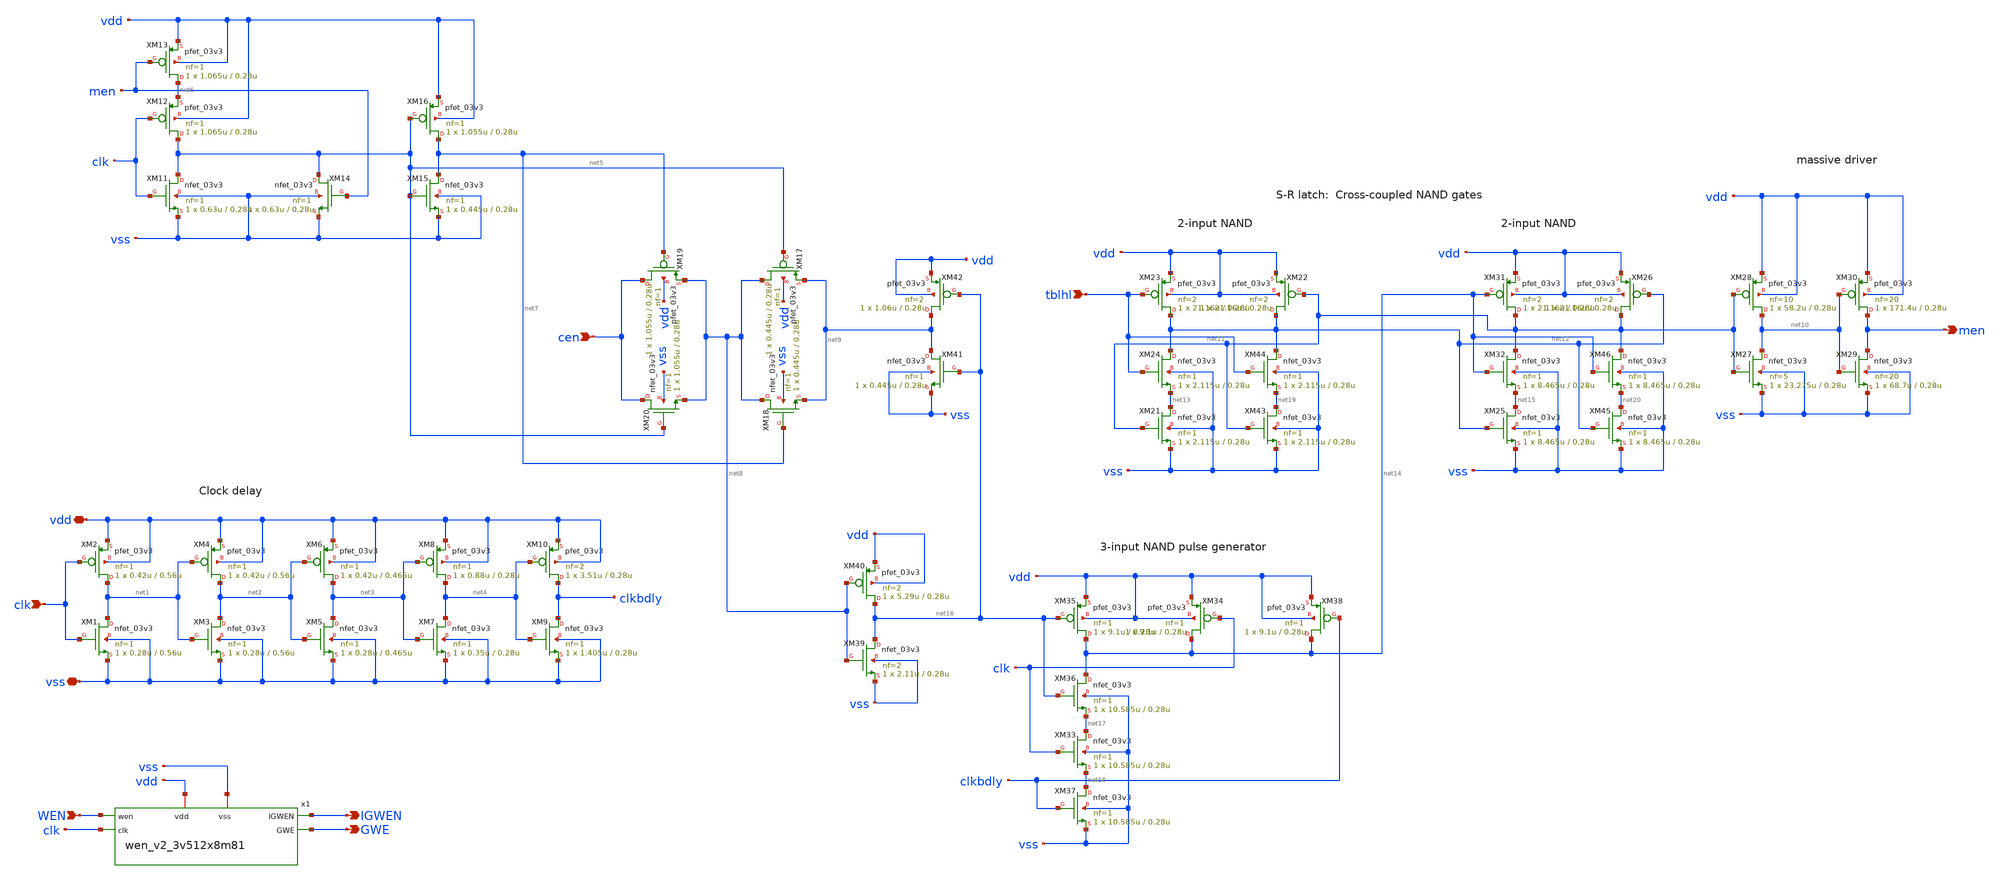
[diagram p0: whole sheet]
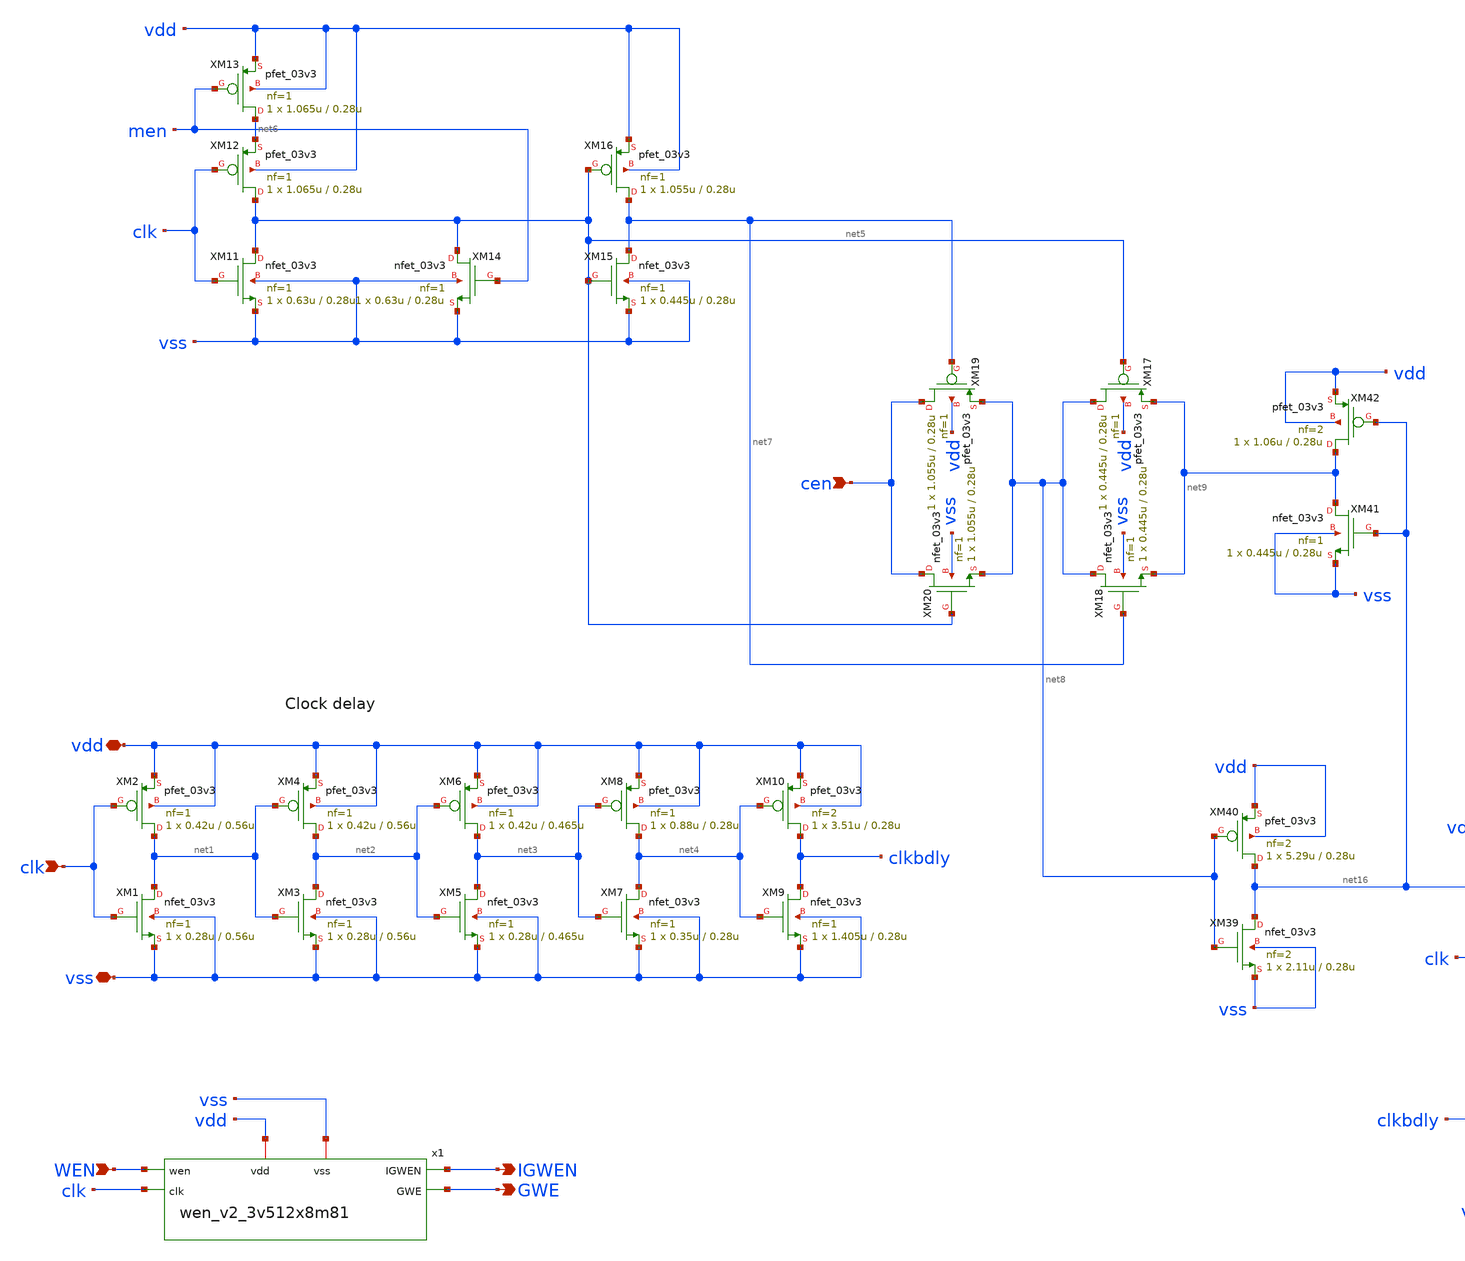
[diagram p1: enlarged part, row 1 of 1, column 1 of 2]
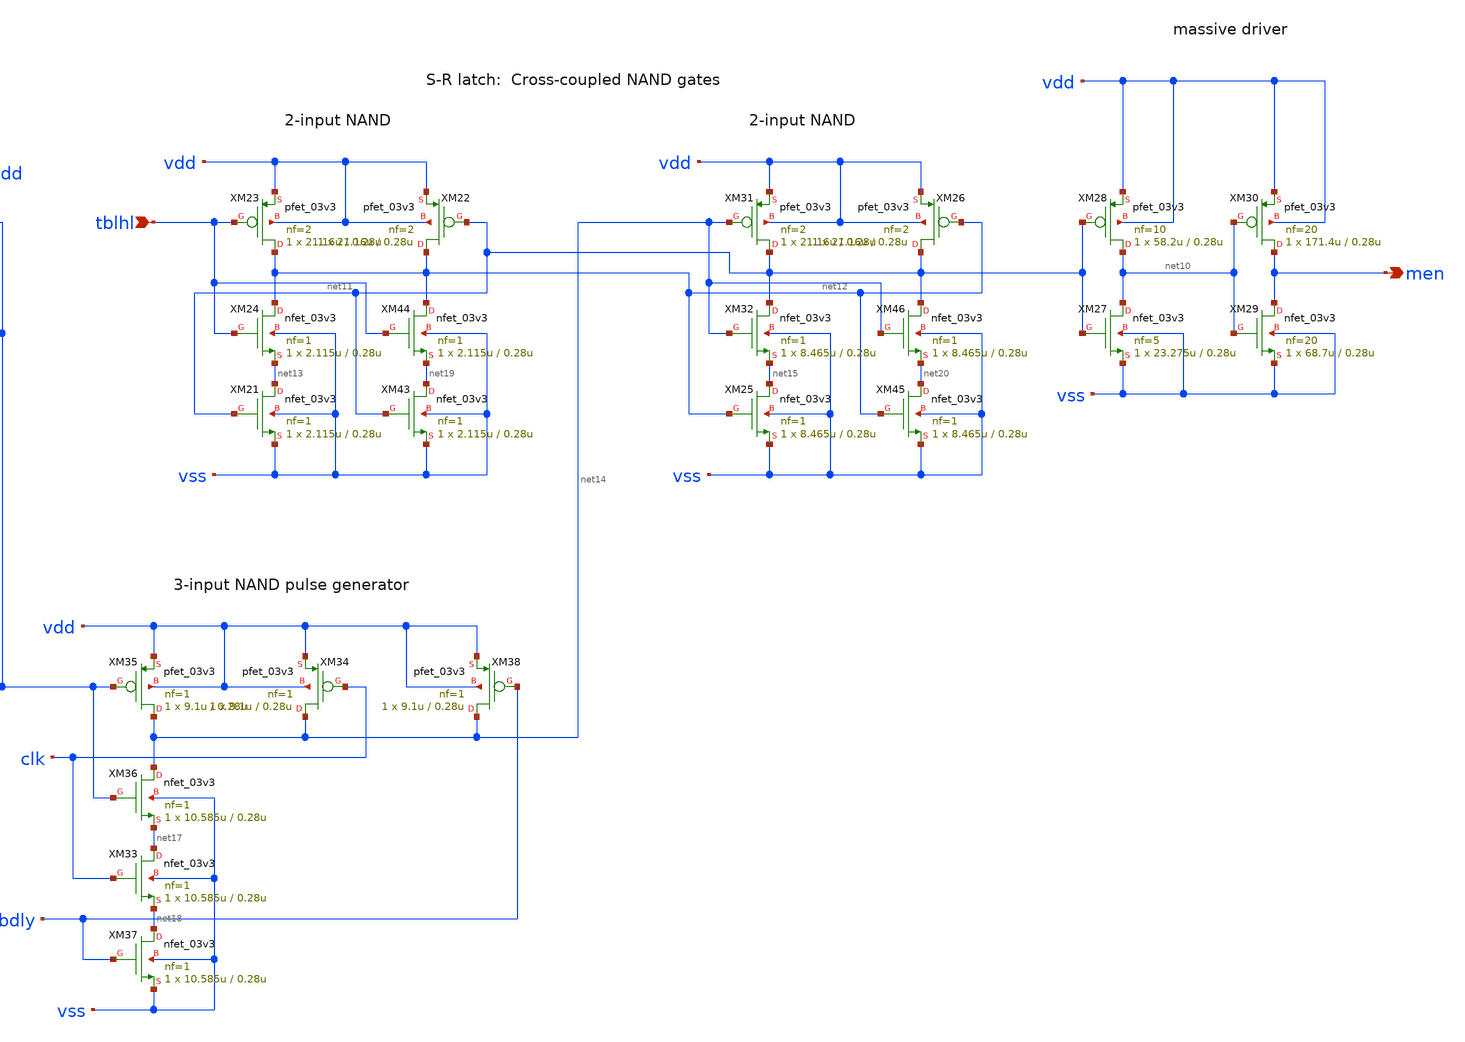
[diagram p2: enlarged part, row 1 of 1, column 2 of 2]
** sch_path: cells/gf180mcu_ocd_ip_sram__sram512x8m8wm1/xschem/gen_3v512x8_3v512x8m81.sch
**.subckt gen_3v512x8_3v512x8m81 clk vdd vss WEN IGWEN GWE men tblhl cen
*.ipin clk
*.iopin vdd
*.iopin vss
*.ipin WEN
*.opin IGWEN
*.opin GWE
*.opin men
*.ipin tblhl
*.ipin cen
XM1 net1 clk vss vss nfet_03v3 L=0.56u W=0.28u nf=1 ad='int((nf+1)/2) * W/nf * 0.18u' as='int((nf+2)/2) * W/nf * 0.18u'
+ pd='2*int((nf+1)/2) * (W/nf + 0.18u)' ps='2*int((nf+2)/2) * (W/nf + 0.18u)' nrd='0.18u / W' nrs='0.18u / W'
+ sa=0 sb=0 sd=0 m=1
XM2 net1 clk vdd vdd pfet_03v3 L=0.56u W=0.42u nf=1 ad='int((nf+1)/2) * W/nf * 0.18u' as='int((nf+2)/2) * W/nf * 0.18u'
+ pd='2*int((nf+1)/2) * (W/nf + 0.18u)' ps='2*int((nf+2)/2) * (W/nf + 0.18u)' nrd='0.18u / W' nrs='0.18u / W'
+ sa=0 sb=0 sd=0 m=1
x1 WEN IGWEN GWE vdd clk vss wen_v2_3v512x8m81
XM5 net3 net2 vss vss nfet_03v3 L=0.465u W=0.28u nf=1 ad='int((nf+1)/2) * W/nf * 0.18u' as='int((nf+2)/2) * W/nf * 0.18u'
+ pd='2*int((nf+1)/2) * (W/nf + 0.18u)' ps='2*int((nf+2)/2) * (W/nf + 0.18u)' nrd='0.18u / W' nrs='0.18u / W'
+ sa=0 sb=0 sd=0 m=1
XM6 net3 net2 vdd vdd pfet_03v3 L=0.465u W=0.42u nf=1 ad='int((nf+1)/2) * W/nf * 0.18u' as='int((nf+2)/2) * W/nf * 0.18u'
+ pd='2*int((nf+1)/2) * (W/nf + 0.18u)' ps='2*int((nf+2)/2) * (W/nf + 0.18u)' nrd='0.18u / W' nrs='0.18u / W'
+ sa=0 sb=0 sd=0 m=1
XM7 net4 net3 vss vss nfet_03v3 L=0.28u W=0.35u nf=1 ad='int((nf+1)/2) * W/nf * 0.18u' as='int((nf+2)/2) * W/nf * 0.18u'
+ pd='2*int((nf+1)/2) * (W/nf + 0.18u)' ps='2*int((nf+2)/2) * (W/nf + 0.18u)' nrd='0.18u / W' nrs='0.18u / W'
+ sa=0 sb=0 sd=0 m=1
XM8 net4 net3 vdd vdd pfet_03v3 L=0.28u W=0.88u nf=1 ad='int((nf+1)/2) * W/nf * 0.18u' as='int((nf+2)/2) * W/nf * 0.18u'
+ pd='2*int((nf+1)/2) * (W/nf + 0.18u)' ps='2*int((nf+2)/2) * (W/nf + 0.18u)' nrd='0.18u / W' nrs='0.18u / W'
+ sa=0 sb=0 sd=0 m=1
XM9 clkbdly net4 vss vss nfet_03v3 L=0.28u W=1.405u nf=1 ad='int((nf+1)/2) * W/nf * 0.18u' as='int((nf+2)/2) * W/nf * 0.18u'
+ pd='2*int((nf+1)/2) * (W/nf + 0.18u)' ps='2*int((nf+2)/2) * (W/nf + 0.18u)' nrd='0.18u / W' nrs='0.18u / W'
+ sa=0 sb=0 sd=0 m=1
XM10 clkbdly net4 vdd vdd pfet_03v3 L=0.28u W=3.51u nf=2 ad='int((nf+1)/2) * W/nf * 0.18u' as='int((nf+2)/2) * W/nf * 0.18u'
+ pd='2*int((nf+1)/2) * (W/nf + 0.18u)' ps='2*int((nf+2)/2) * (W/nf + 0.18u)' nrd='0.18u / W' nrs='0.18u / W'
+ sa=0 sb=0 sd=0 m=1
XM3 net2 net1 vss vss nfet_03v3 L=0.56u W=0.28u nf=1 ad='int((nf+1)/2) * W/nf * 0.18u' as='int((nf+2)/2) * W/nf * 0.18u'
+ pd='2*int((nf+1)/2) * (W/nf + 0.18u)' ps='2*int((nf+2)/2) * (W/nf + 0.18u)' nrd='0.18u / W' nrs='0.18u / W'
+ sa=0 sb=0 sd=0 m=1
XM4 net2 net1 vdd vdd pfet_03v3 L=0.56u W=0.42u nf=1 ad='int((nf+1)/2) * W/nf * 0.18u' as='int((nf+2)/2) * W/nf * 0.18u'
+ pd='2*int((nf+1)/2) * (W/nf + 0.18u)' ps='2*int((nf+2)/2) * (W/nf + 0.18u)' nrd='0.18u / W' nrs='0.18u / W'
+ sa=0 sb=0 sd=0 m=1
XM11 net5 clk vss vss nfet_03v3 L=0.28u W=0.63u nf=1 ad='int((nf+1)/2) * W/nf * 0.18u' as='int((nf+2)/2) * W/nf * 0.18u'
+ pd='2*int((nf+1)/2) * (W/nf + 0.18u)' ps='2*int((nf+2)/2) * (W/nf + 0.18u)' nrd='0.18u / W' nrs='0.18u / W'
+ sa=0 sb=0 sd=0 m=1
XM12 net5 clk net6 vdd pfet_03v3 L=0.28u W=1.065u nf=1 ad='int((nf+1)/2) * W/nf * 0.18u' as='int((nf+2)/2) * W/nf * 0.18u'
+ pd='2*int((nf+1)/2) * (W/nf + 0.18u)' ps='2*int((nf+2)/2) * (W/nf + 0.18u)' nrd='0.18u / W' nrs='0.18u / W'
+ sa=0 sb=0 sd=0 m=1
XM13 net6 men vdd vdd pfet_03v3 L=0.28u W=1.065u nf=1 ad='int((nf+1)/2) * W/nf * 0.18u' as='int((nf+2)/2) * W/nf * 0.18u'
+ pd='2*int((nf+1)/2) * (W/nf + 0.18u)' ps='2*int((nf+2)/2) * (W/nf + 0.18u)' nrd='0.18u / W' nrs='0.18u / W'
+ sa=0 sb=0 sd=0 m=1
XM14 net5 men vss vss nfet_03v3 L=0.28u W=0.63u nf=1 ad='int((nf+1)/2) * W/nf * 0.18u' as='int((nf+2)/2) * W/nf * 0.18u'
+ pd='2*int((nf+1)/2) * (W/nf + 0.18u)' ps='2*int((nf+2)/2) * (W/nf + 0.18u)' nrd='0.18u / W' nrs='0.18u / W'
+ sa=0 sb=0 sd=0 m=1
XM15 net7 net5 vss vss nfet_03v3 L=0.28u W=0.445u nf=1 ad='int((nf+1)/2) * W/nf * 0.18u' as='int((nf+2)/2) * W/nf * 0.18u'
+ pd='2*int((nf+1)/2) * (W/nf + 0.18u)' ps='2*int((nf+2)/2) * (W/nf + 0.18u)' nrd='0.18u / W' nrs='0.18u / W'
+ sa=0 sb=0 sd=0 m=1
XM16 net7 net5 vdd vdd pfet_03v3 L=0.28u W=1.055u nf=1 ad='int((nf+1)/2) * W/nf * 0.18u' as='int((nf+2)/2) * W/nf * 0.18u'
+ pd='2*int((nf+1)/2) * (W/nf + 0.18u)' ps='2*int((nf+2)/2) * (W/nf + 0.18u)' nrd='0.18u / W' nrs='0.18u / W'
+ sa=0 sb=0 sd=0 m=1
XM17 net8 net5 net9 vdd pfet_03v3 L=0.28u W=0.445u nf=1 ad='int((nf+1)/2) * W/nf * 0.18u' as='int((nf+2)/2) * W/nf * 0.18u'
+ pd='2*int((nf+1)/2) * (W/nf + 0.18u)' ps='2*int((nf+2)/2) * (W/nf + 0.18u)' nrd='0.18u / W' nrs='0.18u / W'
+ sa=0 sb=0 sd=0 m=1
XM18 net8 net7 net9 vss nfet_03v3 L=0.28u W=0.445u nf=1 ad='int((nf+1)/2) * W/nf * 0.18u' as='int((nf+2)/2) * W/nf * 0.18u'
+ pd='2*int((nf+1)/2) * (W/nf + 0.18u)' ps='2*int((nf+2)/2) * (W/nf + 0.18u)' nrd='0.18u / W' nrs='0.18u / W'
+ sa=0 sb=0 sd=0 m=1
XM19 cen net7 net8 vdd pfet_03v3 L=0.28u W=1.055u nf=1 ad='int((nf+1)/2) * W/nf * 0.18u' as='int((nf+2)/2) * W/nf * 0.18u'
+ pd='2*int((nf+1)/2) * (W/nf + 0.18u)' ps='2*int((nf+2)/2) * (W/nf + 0.18u)' nrd='0.18u / W' nrs='0.18u / W'
+ sa=0 sb=0 sd=0 m=1
XM20 cen net5 net8 vss nfet_03v3 L=0.28u W=1.055u nf=1 ad='int((nf+1)/2) * W/nf * 0.18u' as='int((nf+2)/2) * W/nf * 0.18u'
+ pd='2*int((nf+1)/2) * (W/nf + 0.18u)' ps='2*int((nf+2)/2) * (W/nf + 0.18u)' nrd='0.18u / W' nrs='0.18u / W'
+ sa=0 sb=0 sd=0 m=1
XM21 net13 net11 vss vss nfet_03v3 L=0.28u W=2.115u nf=1 ad='int((nf+1)/2) * W/nf * 0.18u' as='int((nf+2)/2) * W/nf * 0.18u'
+ pd='2*int((nf+1)/2) * (W/nf + 0.18u)' ps='2*int((nf+2)/2) * (W/nf + 0.18u)' nrd='0.18u / W' nrs='0.18u / W'
+ sa=0 sb=0 sd=0 m=1
XM22 net12 net11 vdd vdd pfet_03v3 L=0.28u W=21.16u nf=2 ad='int((nf+1)/2) * W/nf * 0.18u' as='int((nf+2)/2) * W/nf * 0.18u'
+ pd='2*int((nf+1)/2) * (W/nf + 0.18u)' ps='2*int((nf+2)/2) * (W/nf + 0.18u)' nrd='0.18u / W' nrs='0.18u / W'
+ sa=0 sb=0 sd=0 m=1
XM23 net12 tblhl vdd vdd pfet_03v3 L=0.28u W=21.16u nf=2 ad='int((nf+1)/2) * W/nf * 0.18u' as='int((nf+2)/2) * W/nf * 0.18u'
+ pd='2*int((nf+1)/2) * (W/nf + 0.18u)' ps='2*int((nf+2)/2) * (W/nf + 0.18u)' nrd='0.18u / W' nrs='0.18u / W'
+ sa=0 sb=0 sd=0 m=1
XM24 net12 tblhl net13 vss nfet_03v3 L=0.28u W=2.115u nf=1 ad='int((nf+1)/2) * W/nf * 0.18u' as='int((nf+2)/2) * W/nf * 0.18u'
+ pd='2*int((nf+1)/2) * (W/nf + 0.18u)' ps='2*int((nf+2)/2) * (W/nf + 0.18u)' nrd='0.18u / W' nrs='0.18u / W'
+ sa=0 sb=0 sd=0 m=1
XM27 net10 net11 vss vss nfet_03v3 L=0.28u W=23.275u nf=5 ad='int((nf+1)/2) * W/nf * 0.18u' as='int((nf+2)/2) * W/nf * 0.18u'
+ pd='2*int((nf+1)/2) * (W/nf + 0.18u)' ps='2*int((nf+2)/2) * (W/nf + 0.18u)' nrd='0.18u / W' nrs='0.18u / W'
+ sa=0 sb=0 sd=0 m=1
XM28 net10 net11 vdd vdd pfet_03v3 L=0.28u W=58.2u nf=10 ad='int((nf+1)/2) * W/nf * 0.18u' as='int((nf+2)/2) * W/nf * 0.18u'
+ pd='2*int((nf+1)/2) * (W/nf + 0.18u)' ps='2*int((nf+2)/2) * (W/nf + 0.18u)' nrd='0.18u / W' nrs='0.18u / W'
+ sa=0 sb=0 sd=0 m=1
XM29 men net10 vss vss nfet_03v3 L=0.28u W=68.7u nf=20 ad='int((nf+1)/2) * W/nf * 0.18u' as='int((nf+2)/2) * W/nf * 0.18u'
+ pd='2*int((nf+1)/2) * (W/nf + 0.18u)' ps='2*int((nf+2)/2) * (W/nf + 0.18u)' nrd='0.18u / W' nrs='0.18u / W'
+ sa=0 sb=0 sd=0 m=1
XM30 men net10 vdd vdd pfet_03v3 L=0.28u W=171.4u nf=20 ad='int((nf+1)/2) * W/nf * 0.18u' as='int((nf+2)/2) * W/nf * 0.18u'
+ pd='2*int((nf+1)/2) * (W/nf + 0.18u)' ps='2*int((nf+2)/2) * (W/nf + 0.18u)' nrd='0.18u / W' nrs='0.18u / W'
+ sa=0 sb=0 sd=0 m=1
XM25 net15 net12 vss vss nfet_03v3 L=0.28u W=8.465u nf=1 ad='int((nf+1)/2) * W/nf * 0.18u' as='int((nf+2)/2) * W/nf * 0.18u'
+ pd='2*int((nf+1)/2) * (W/nf + 0.18u)' ps='2*int((nf+2)/2) * (W/nf + 0.18u)' nrd='0.18u / W' nrs='0.18u / W'
+ sa=0 sb=0 sd=0 m=1
XM26 net11 net12 vdd vdd pfet_03v3 L=0.28u W=21.16u nf=2 ad='int((nf+1)/2) * W/nf * 0.18u' as='int((nf+2)/2) * W/nf * 0.18u'
+ pd='2*int((nf+1)/2) * (W/nf + 0.18u)' ps='2*int((nf+2)/2) * (W/nf + 0.18u)' nrd='0.18u / W' nrs='0.18u / W'
+ sa=0 sb=0 sd=0 m=1
XM31 net11 net14 vdd vdd pfet_03v3 L=0.28u W=21.16u nf=2 ad='int((nf+1)/2) * W/nf * 0.18u' as='int((nf+2)/2) * W/nf * 0.18u'
+ pd='2*int((nf+1)/2) * (W/nf + 0.18u)' ps='2*int((nf+2)/2) * (W/nf + 0.18u)' nrd='0.18u / W' nrs='0.18u / W'
+ sa=0 sb=0 sd=0 m=1
XM32 net11 net14 net15 vss nfet_03v3 L=0.28u W=8.465u nf=1 ad='int((nf+1)/2) * W/nf * 0.18u' as='int((nf+2)/2) * W/nf * 0.18u'
+ pd='2*int((nf+1)/2) * (W/nf + 0.18u)' ps='2*int((nf+2)/2) * (W/nf + 0.18u)' nrd='0.18u / W' nrs='0.18u / W'
+ sa=0 sb=0 sd=0 m=1
XM35 net14 net16 vdd vdd pfet_03v3 L=0.28u W=9.1u nf=1 ad='int((nf+1)/2) * W/nf * 0.18u' as='int((nf+2)/2) * W/nf * 0.18u'
+ pd='2*int((nf+1)/2) * (W/nf + 0.18u)' ps='2*int((nf+2)/2) * (W/nf + 0.18u)' nrd='0.18u / W' nrs='0.18u / W'
+ sa=0 sb=0 sd=0 m=1
XM36 net14 net16 net17 vss nfet_03v3 L=0.28u W=10.585u nf=1 ad='int((nf+1)/2) * W/nf * 0.18u' as='int((nf+2)/2) * W/nf * 0.18u'
+ pd='2*int((nf+1)/2) * (W/nf + 0.18u)' ps='2*int((nf+2)/2) * (W/nf + 0.18u)' nrd='0.18u / W' nrs='0.18u / W'
+ sa=0 sb=0 sd=0 m=1
XM33 net17 clk net18 vss nfet_03v3 L=0.28u W=10.585u nf=1 ad='int((nf+1)/2) * W/nf * 0.18u' as='int((nf+2)/2) * W/nf * 0.18u'
+ pd='2*int((nf+1)/2) * (W/nf + 0.18u)' ps='2*int((nf+2)/2) * (W/nf + 0.18u)' nrd='0.18u / W' nrs='0.18u / W'
+ sa=0 sb=0 sd=0 m=1
XM37 net18 clkbdly vss vss nfet_03v3 L=0.28u W=10.585u nf=1 ad='int((nf+1)/2) * W/nf * 0.18u' as='int((nf+2)/2) * W/nf * 0.18u'
+ pd='2*int((nf+1)/2) * (W/nf + 0.18u)' ps='2*int((nf+2)/2) * (W/nf + 0.18u)' nrd='0.18u / W' nrs='0.18u / W'
+ sa=0 sb=0 sd=0 m=1
XM34 net14 clk vdd vdd pfet_03v3 L=0.28u W=9.1u nf=1 ad='int((nf+1)/2) * W/nf * 0.18u' as='int((nf+2)/2) * W/nf * 0.18u'
+ pd='2*int((nf+1)/2) * (W/nf + 0.18u)' ps='2*int((nf+2)/2) * (W/nf + 0.18u)' nrd='0.18u / W' nrs='0.18u / W'
+ sa=0 sb=0 sd=0 m=1
XM38 net14 clkbdly vdd vdd pfet_03v3 L=0.28u W=9.1u nf=1 ad='int((nf+1)/2) * W/nf * 0.18u' as='int((nf+2)/2) * W/nf * 0.18u'
+ pd='2*int((nf+1)/2) * (W/nf + 0.18u)' ps='2*int((nf+2)/2) * (W/nf + 0.18u)' nrd='0.18u / W' nrs='0.18u / W'
+ sa=0 sb=0 sd=0 m=1
XM39 net16 net8 vss vss nfet_03v3 L=0.28u W=2.11u nf=2 ad='int((nf+1)/2) * W/nf * 0.18u' as='int((nf+2)/2) * W/nf * 0.18u'
+ pd='2*int((nf+1)/2) * (W/nf + 0.18u)' ps='2*int((nf+2)/2) * (W/nf + 0.18u)' nrd='0.18u / W' nrs='0.18u / W'
+ sa=0 sb=0 sd=0 m=1
XM40 net16 net8 vdd vdd pfet_03v3 L=0.28u W=5.29u nf=2 ad='int((nf+1)/2) * W/nf * 0.18u' as='int((nf+2)/2) * W/nf * 0.18u'
+ pd='2*int((nf+1)/2) * (W/nf + 0.18u)' ps='2*int((nf+2)/2) * (W/nf + 0.18u)' nrd='0.18u / W' nrs='0.18u / W'
+ sa=0 sb=0 sd=0 m=1
XM41 net9 net16 vss vss nfet_03v3 L=0.28u W=0.445u nf=1 ad='int((nf+1)/2) * W/nf * 0.18u' as='int((nf+2)/2) * W/nf * 0.18u'
+ pd='2*int((nf+1)/2) * (W/nf + 0.18u)' ps='2*int((nf+2)/2) * (W/nf + 0.18u)' nrd='0.18u / W' nrs='0.18u / W'
+ sa=0 sb=0 sd=0 m=1
XM42 net9 net16 vdd vdd pfet_03v3 L=0.28u W=1.06u nf=2 ad='int((nf+1)/2) * W/nf * 0.18u' as='int((nf+2)/2) * W/nf * 0.18u'
+ pd='2*int((nf+1)/2) * (W/nf + 0.18u)' ps='2*int((nf+2)/2) * (W/nf + 0.18u)' nrd='0.18u / W' nrs='0.18u / W'
+ sa=0 sb=0 sd=0 m=1
XM43 net19 net11 vss vss nfet_03v3 L=0.28u W=2.115u nf=1 ad='int((nf+1)/2) * W/nf * 0.18u' as='int((nf+2)/2) * W/nf * 0.18u'
+ pd='2*int((nf+1)/2) * (W/nf + 0.18u)' ps='2*int((nf+2)/2) * (W/nf + 0.18u)' nrd='0.18u / W' nrs='0.18u / W'
+ sa=0 sb=0 sd=0 m=1
XM44 net12 tblhl net19 vss nfet_03v3 L=0.28u W=2.115u nf=1 ad='int((nf+1)/2) * W/nf * 0.18u' as='int((nf+2)/2) * W/nf * 0.18u'
+ pd='2*int((nf+1)/2) * (W/nf + 0.18u)' ps='2*int((nf+2)/2) * (W/nf + 0.18u)' nrd='0.18u / W' nrs='0.18u / W'
+ sa=0 sb=0 sd=0 m=1
XM45 net20 net12 vss vss nfet_03v3 L=0.28u W=8.465u nf=1 ad='int((nf+1)/2) * W/nf * 0.18u' as='int((nf+2)/2) * W/nf * 0.18u'
+ pd='2*int((nf+1)/2) * (W/nf + 0.18u)' ps='2*int((nf+2)/2) * (W/nf + 0.18u)' nrd='0.18u / W' nrs='0.18u / W'
+ sa=0 sb=0 sd=0 m=1
XM46 net11 net14 net20 vss nfet_03v3 L=0.28u W=8.465u nf=1 ad='int((nf+1)/2) * W/nf * 0.18u' as='int((nf+2)/2) * W/nf * 0.18u'
+ pd='2*int((nf+1)/2) * (W/nf + 0.18u)' ps='2*int((nf+2)/2) * (W/nf + 0.18u)' nrd='0.18u / W' nrs='0.18u / W'
+ sa=0 sb=0 sd=0 m=1
**.ends
.end
